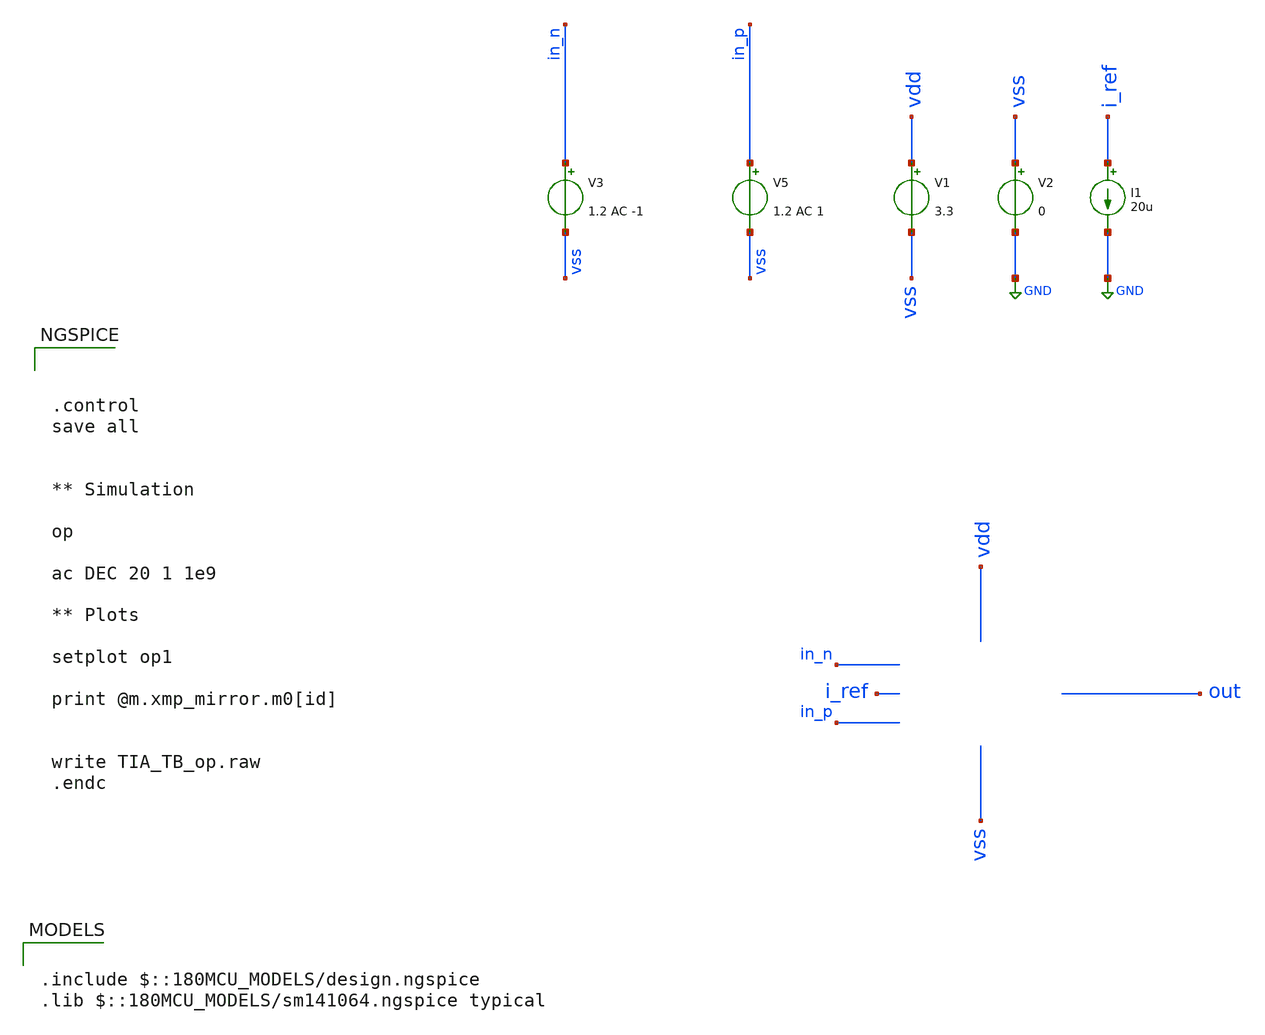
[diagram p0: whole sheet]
** sch_path: designs/libs/TIA/TIA_TB_ac.sch
**.subckt TIA_TB_ac
V1 vdd vss 3.3
V2 vss GND 0
V3 in_n vss 1.2 AC -1
V5 in_p vss 1.2 AC 1
I1 i_ref GND 20u
**** begin user architecture code



.control
save all


** Simulation

op

ac DEC 20 1 1e9

** Plots

setplot op1

print @m.xmp_mirror.m0[id]


write TIA_TB_op.raw
.endc



.include $::180MCU_MODELS/design.ngspice
.lib $::180MCU_MODELS/sm141064.ngspice typical

**** end user architecture code
**.ends
.GLOBAL GND
.end
